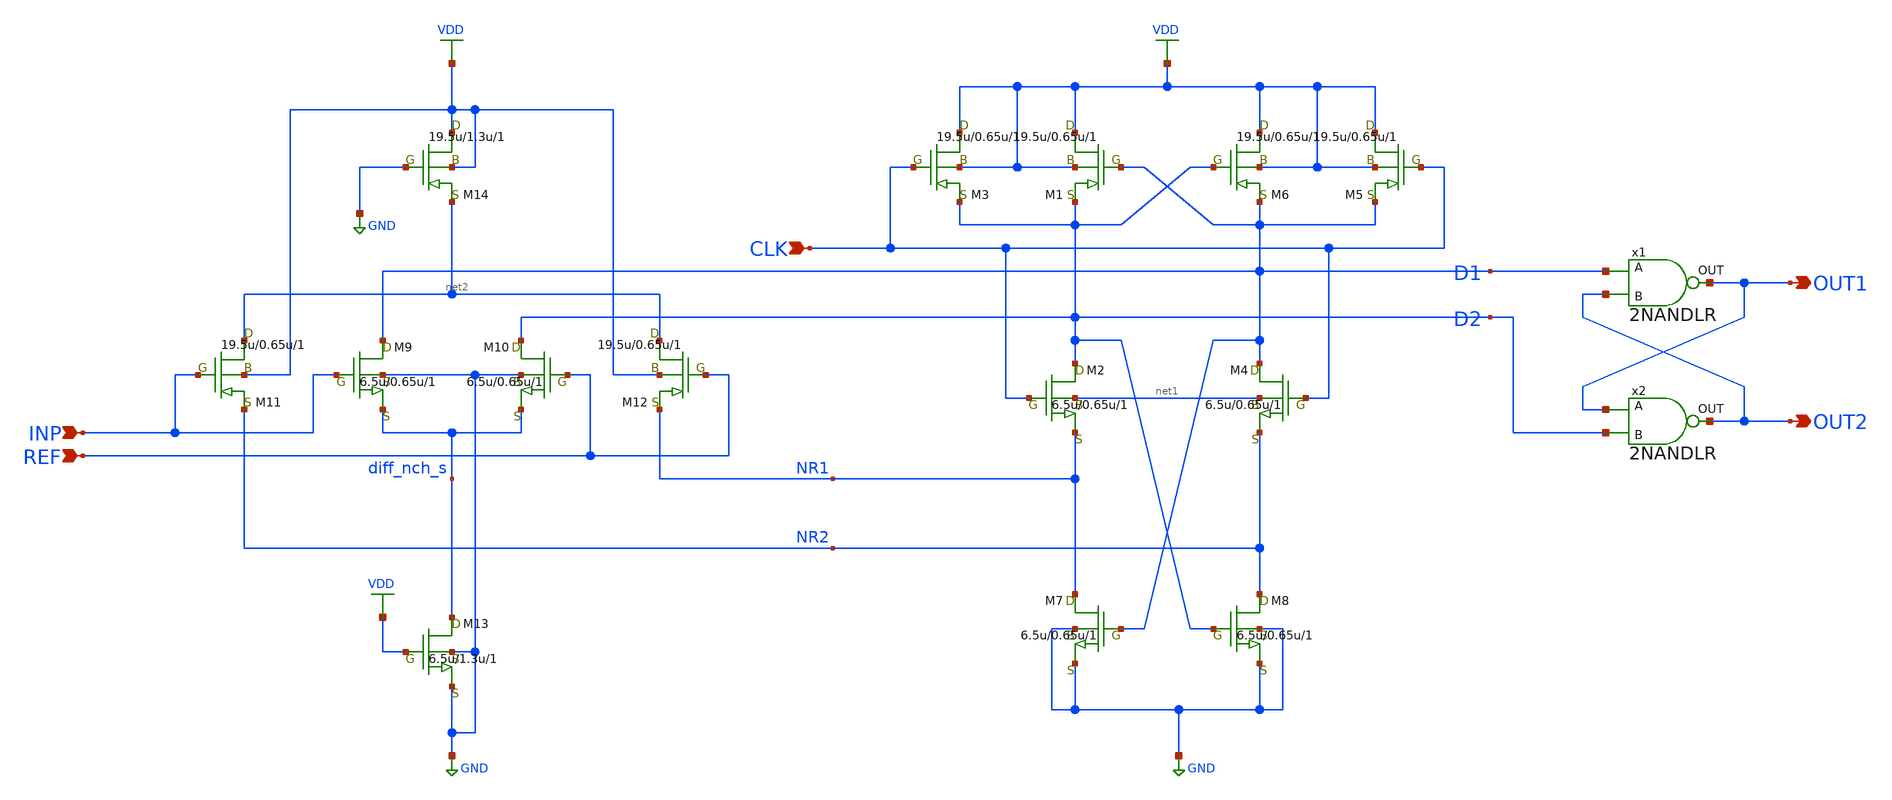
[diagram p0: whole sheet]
** sch_path: outdata/LR_hokari/LR_Work2/Wide-swing_clocked_comparator.sch
**.subckt Wide-swing_clocked_comparator INP REF CLK OUT1 OUT2
*.ipin INP
*.ipin REF
*.ipin CLK
*.opin OUT1
*.opin OUT2
M2 D2 CLK NR1 net1 nch w=6.5u l=0.65u as=0 ps=0 ad=0 pd=0 m=1
M4 D1 CLK NR2 net1 nch w=6.5u l=0.65u as=0 ps=0 ad=0 pd=0 m=1
M5 VDD CLK D1 VDD pch w=19.5u l=0.65u as=0 ps=0 ad=0 pd=0 m=1
M6 VDD D2 D1 VDD pch w=19.5u l=0.65u as=0 ps=0 ad=0 pd=0 m=1
M7 NR1 D1 GND GND nch w=6.5u l=0.65u as=0 ps=0 ad=0 pd=0 m=1
M8 NR2 D2 GND GND nch w=6.5u l=0.65u as=0 ps=0 ad=0 pd=0 m=1
x1 D1 OUT1 OUT2 2NANDLR
x2 OUT1 OUT2 D2 2NANDLR
M1 VDD D1 D2 VDD pch w=19.5u l=0.65u as=0 ps=0 ad=0 pd=0 m=1
M3 VDD CLK D2 VDD pch w=19.5u l=0.65u as=0 ps=0 ad=0 pd=0 m=1
M12 net2 REF NR1 VDD pch w=19.5u l=0.65u as=0 ps=0 ad=0 pd=0 m=1
M11 net2 INP NR2 VDD pch w=19.5u l=0.65u as=0 ps=0 ad=0 pd=0 m=1
M9 D1 INP diff_nch_s GND nch w=6.5u l=0.65u as=0 ps=0 ad=0 pd=0 m=1
M10 D2 REF diff_nch_s GND nch w=6.5u l=0.65u as=0 ps=0 ad=0 pd=0 m=1
M13 diff_nch_s VDD GND GND nch w=6.5u l=1.3u as=0 ps=0 ad=0 pd=0 m=1
M14 VDD GND net2 VDD pch w=19.5u l=1.3u as=0 ps=0 ad=0 pd=0 m=1
**** begin user architecture code



.inc /home/tororo/LR/T_mos_model.sp

VVDD VDD 0 DC 3.3

VINP INP 0 pwl (0 0 25n 0 26n 3.3 75n 3.3 76n 0.2 125n 0.2 126n 3.1 175n 3.1 176n 0.4 225n 0.4 226n
+ 2.9 275n 2.9 276n 0.6 325n 0.6 326n 2.7 375n 2.7 376n 0.8 425n 0.8 426n 2.5 475n 2.5 476n 1.0 525n 1.0
+ 526n 2.3 575n 2.3 576n 1.2 625n 1.2   626n 2.1 675n 2.1 +676n 1.4 725n 1.4 726n 1.9 775n 1.9 776n 1.6
+ 825n 1.6 826n 1.7 875n 1.7 )
*VINP INP 0 pwl (0 0 25n 0 26n 1.7 75n 1.7 76n 1.6 125n 1.6 126n 1.68 175n 1.68 176n 1.62 225n 1.62
*+ 226n 1.66 275n 1.66 276n 1.64 325n 1.64 326n 1.655 375n 1.655 376n 1.645 425n 1.645 426n 1.651 475n
*+ 1.651 476n 1.649 525n 1.649 526n 1.6501 575n 1.6501 576n 1.6499 625n 1.6499 626n 1.65001 675n 1.65001
*+ 676n 1.64999 725n 1.6499 726n 1.9 775n 1.9 776n 1.6 825n 1.6 826n 1.7 875n 1.7)
*VINP INP 0 pwl (0 2.15 25n 2.15 26n 1.15 75n 1.15 76n 1.95 125n 1.95 126n 1.35 175n 1.35)
*VINP INP 0 pwl (0 1.85 25n 1.85 26n 1.45 75n 1.45 76n 1.83 125n 1.83 126n 1.47 175n 1.47)

VREF REF 0 DC 1.65

VCLK CLK 0 pulse(0 3.3 0n 1n 1n 25n 50n)
*VCLK CLK 0 pulse(0 3.3 0n 1n 1n 50n 100n)

.control
tran 1n 875n

*meas tran delayIN1 find time WHEN v(CLK)=0.9 RISE=3
*meas tran delayOUT find time WHEN v(OUT1)=0.9 FALL=2
*let delay1 = delayOUT - delayIN1
*echo tpHL = $&delay1

*meas tran delayIN1 find time WHEN v(CLK)=0.9 RISE=4
*meas tran delayOUT find time WHEN v(OUT1)=0.9 RISE=2
*let delay2 = delayOUT - delayIN1
*echo tpLH = $&delay2


write Wide-swing_clocked_comparator.raw

.endc

**** end user architecture code
**.ends

* expanding   symbol:  LR_Work2/symbol/2NANDLR.sym # of pins=3
** sym_path: LR_hokari/LR_Work2/symbol/2NANDLR.sym
** sch_path: LR_hokari/LR_Work2/symbol/2NANDLR.sch
.subckt 2NANDLR A OUT B
*.ipin A
*.ipin B
*.opin OUT
M1 OUT A net1 GND nch w=3.5u l=3.5u as=0 ps=0 ad=0 pd=0 m=1
M2 OUT B VDD VDD pch w=10.5u l=3.5u as=0 ps=0 ad=0 pd=0 m=1
M3 OUT A VDD VDD pch w=10.5u l=3.5u as=0 ps=0 ad=0 pd=0 m=1
M4 net1 B GND GND nch w=3.5u l=10.5u as=0 ps=0 ad=0 pd=0 m=1
.ends

.GLOBAL VDD
.GLOBAL GND
.end
